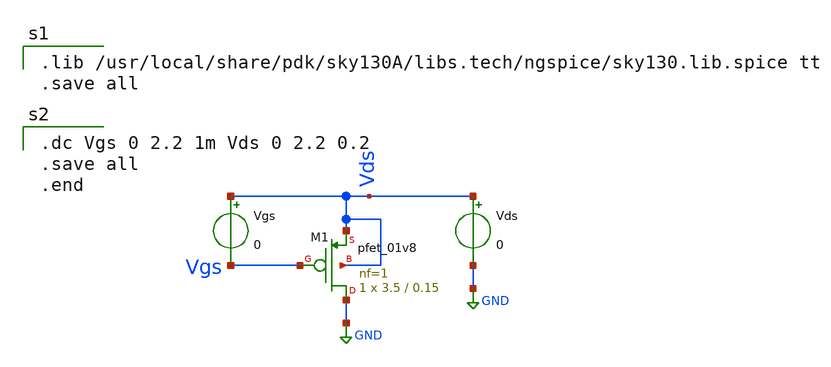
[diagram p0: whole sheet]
** sch_path: OneDrive/Documents/CMOS-Inverter-Design-and-Analysis-using-Sky130pdk-main/xschem/pmos_01v8.sch
**.subckt pmos_01v8
XM1 GND Vgs Vds Vds sky130_fd_pr__pfet_01v8 L=0.15 W=3.5 nf=1 ad='int((1 + 1)/2) * 3.5 / 1 * 0.29' as='int((1 + 2)/2) * 3.5 / 1 * 0.29'
+ pd='2*int((1 + 1)/2) * (3.5 / 1 + 0.29)' ps='2*int((1 + 2)/2) * (3.5 / 1 + 0.29)' nrd='0.29 / 3.5 ' nrs='0.29 / 3.5 '
+ sa=0 sb=0 sd=0 mult=1 m=1
Vds Vds GND 0
Vgs Vds Vgs 0
**** begin user architecture code

.lib /usr/local/share/pdk/sky130A/libs.tech/ngspice/sky130.lib.spice tt
.save all


.dc Vgs 0 2.2 1m Vds 0 2.2 0.2
.save all
.end

**** end user architecture code
**.ends
.GLOBAL GND
.end
